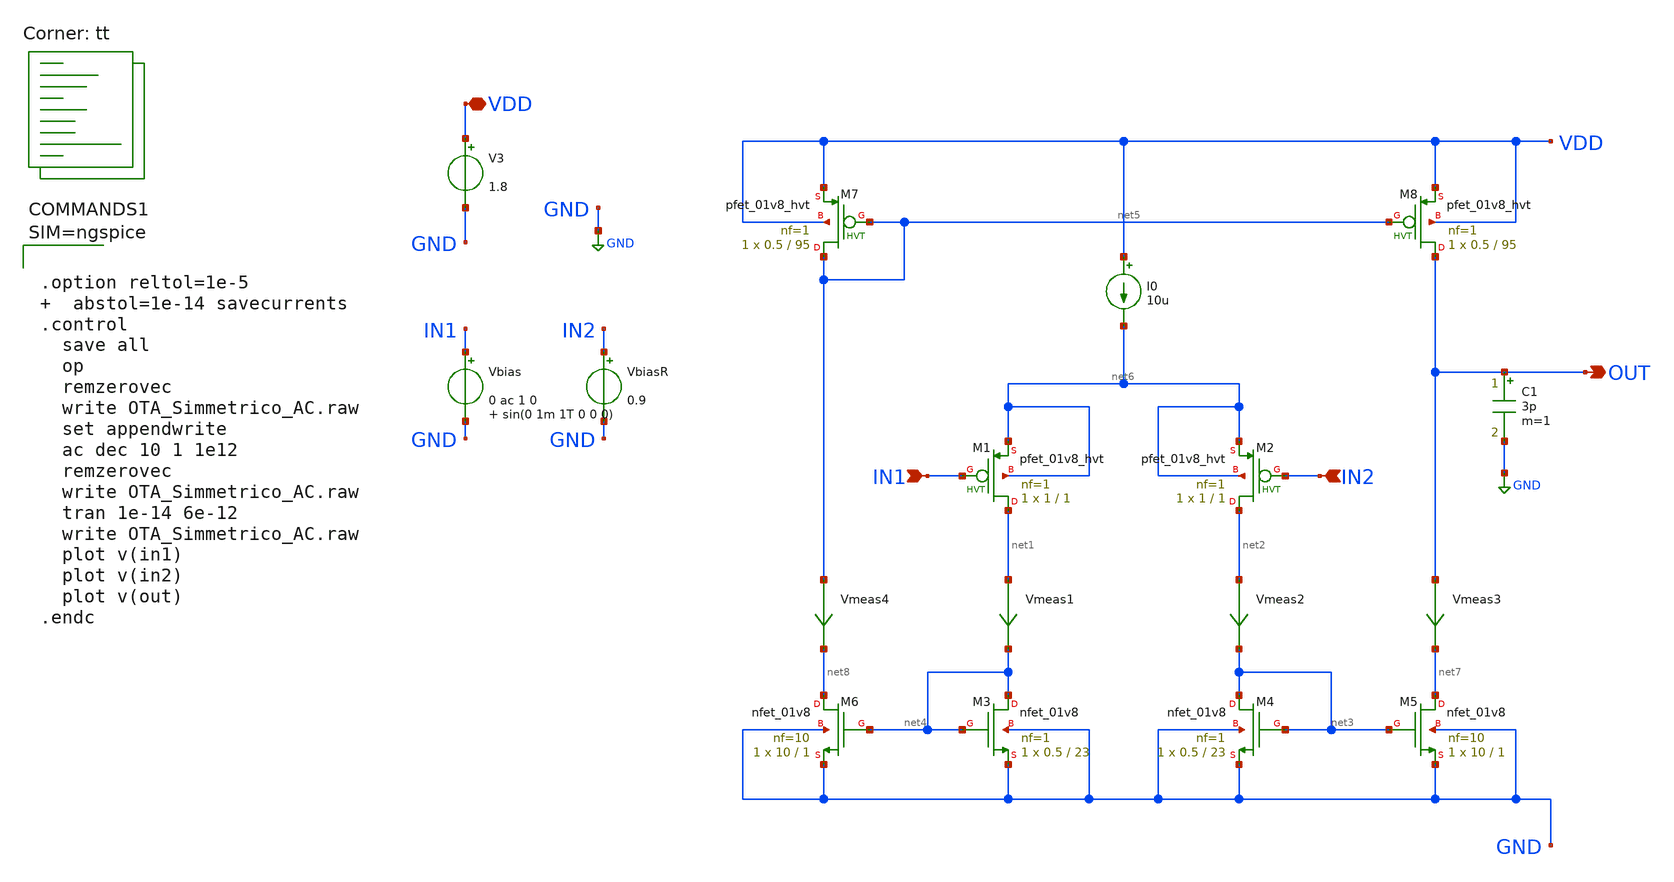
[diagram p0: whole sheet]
** sch_path: xschem/OTA_Simmetrico_AC.sch
**.subckt OTA_Simmetrico_AC VDD IN1 IN2 OUT
*.iopin VDD
*.ipin IN1
*.ipin IN2
*.opin OUT
V3 VDD GND 1.8
Vbias IN1 GND 0 ac 1 0 sin(0 1m 1T 0 0 0)
VbiasR IN2 GND 0.9
XM1 net1 IN1 net6 net6 sky130_fd_pr__pfet_01v8_hvt L=1 W=1 nf=1 ad='int((nf+1)/2) * W/nf * 0.29' as='int((nf+2)/2) * W/nf * 0.29'
+ pd='2*int((nf+1)/2) * (W/nf + 0.29)' ps='2*int((nf+2)/2) * (W/nf + 0.29)' nrd='0.29 / W' nrs='0.29 / W'
+ sa=0 sb=0 sd=0 mult=1 m=1
XM2 net2 IN2 net6 net6 sky130_fd_pr__pfet_01v8_hvt L=1 W=1 nf=1 ad='int((nf+1)/2) * W/nf * 0.29' as='int((nf+2)/2) * W/nf * 0.29'
+ pd='2*int((nf+1)/2) * (W/nf + 0.29)' ps='2*int((nf+2)/2) * (W/nf + 0.29)' nrd='0.29 / W' nrs='0.29 / W'
+ sa=0 sb=0 sd=0 mult=1 m=1
XM3 net4 net4 GND GND sky130_fd_pr__nfet_01v8 L=23 W=0.5 nf=1 ad='int((nf+1)/2) * W/nf * 0.29' as='int((nf+2)/2) * W/nf * 0.29'
+ pd='2*int((nf+1)/2) * (W/nf + 0.29)' ps='2*int((nf+2)/2) * (W/nf + 0.29)' nrd='0.29 / W' nrs='0.29 / W'
+ sa=0 sb=0 sd=0 mult=1 m=1
XM4 net3 net3 GND GND sky130_fd_pr__nfet_01v8 L=23 W=0.5 nf=1 ad='int((nf+1)/2) * W/nf * 0.29' as='int((nf+2)/2) * W/nf * 0.29'
+ pd='2*int((nf+1)/2) * (W/nf + 0.29)' ps='2*int((nf+2)/2) * (W/nf + 0.29)' nrd='0.29 / W' nrs='0.29 / W'
+ sa=0 sb=0 sd=0 mult=1 m=1
XM5 net7 net3 GND GND sky130_fd_pr__nfet_01v8 L=1 W=10 nf=10 ad='int((nf+1)/2) * W/nf * 0.29' as='int((nf+2)/2) * W/nf * 0.29'
+ pd='2*int((nf+1)/2) * (W/nf + 0.29)' ps='2*int((nf+2)/2) * (W/nf + 0.29)' nrd='0.29 / W' nrs='0.29 / W'
+ sa=0 sb=0 sd=0 mult=1 m=1
XM6 net8 net4 GND GND sky130_fd_pr__nfet_01v8 L=1 W=10 nf=10 ad='int((nf+1)/2) * W/nf * 0.29' as='int((nf+2)/2) * W/nf * 0.29'
+ pd='2*int((nf+1)/2) * (W/nf + 0.29)' ps='2*int((nf+2)/2) * (W/nf + 0.29)' nrd='0.29 / W' nrs='0.29 / W'
+ sa=0 sb=0 sd=0 mult=1 m=1
XM7 net5 net5 VDD VDD sky130_fd_pr__pfet_01v8_hvt L=95 W=0.5 nf=1 ad='int((nf+1)/2) * W/nf * 0.29' as='int((nf+2)/2) * W/nf * 0.29'
+ pd='2*int((nf+1)/2) * (W/nf + 0.29)' ps='2*int((nf+2)/2) * (W/nf + 0.29)' nrd='0.29 / W' nrs='0.29 / W'
+ sa=0 sb=0 sd=0 mult=1 m=1
XM8 OUT net5 VDD VDD sky130_fd_pr__pfet_01v8_hvt L=95 W=0.5 nf=1 ad='int((nf+1)/2) * W/nf * 0.29' as='int((nf+2)/2) * W/nf * 0.29'
+ pd='2*int((nf+1)/2) * (W/nf + 0.29)' ps='2*int((nf+2)/2) * (W/nf + 0.29)' nrd='0.29 / W' nrs='0.29 / W'
+ sa=0 sb=0 sd=0 mult=1 m=1
Vmeas1 net1 net4 0
.save i(vmeas1)
Vmeas2 net2 net3 0
.save i(vmeas2)
Vmeas3 OUT net7 0
.save i(vmeas3)
Vmeas4 net5 net8 0
.save i(vmeas4)
I0 VDD net6 10u
C1 OUT GND 3p m=1
**** begin user architecture code
.lib $::SKYWATER_MODELS/sky130.lib.spice tt



.option reltol=1e-5   abstol=1e-14 savecurrents
.control
  save all
  op
  remzerovec
  write OTA_Simmetrico_AC.raw
  set appendwrite
  ac dec 10 1 1e12
  remzerovec
  write OTA_Simmetrico_AC.raw
  tran 1e-14 6e-12
  write OTA_Simmetrico_AC.raw
  plot v(in1)
  plot v(in2)
  plot v(out)
.endc



**** end user architecture code
**.ends
.GLOBAL GND
.end
